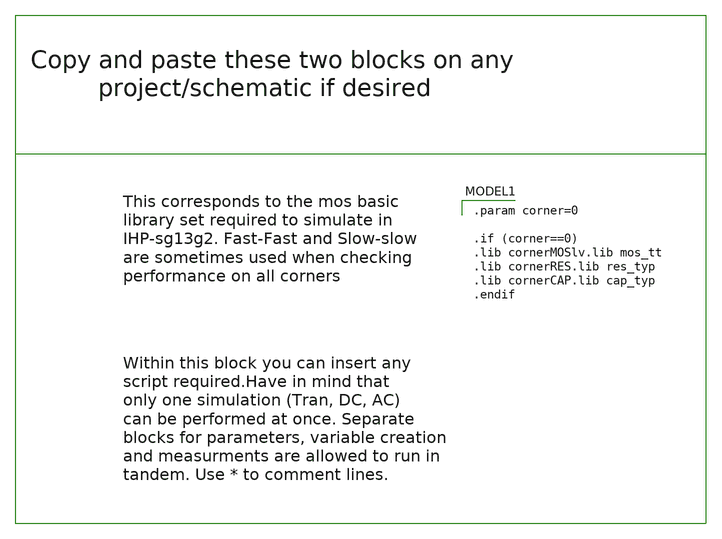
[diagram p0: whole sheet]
** sch_path: Tutoriales/Simulation_fundamentals.sch
**.subckt Simulation_fundamentals
**** begin user architecture code
 .param corner=0

.if (corner==0)
.lib cornerMOSlv.lib mos_tt
.lib cornerRES.lib res_typ
.lib cornerCAP.lib cap_typ
.endif




*At this point the script is to be written. Before the .control command, you can
* Declare Netlist components
* Declare parameters for later use
* Set voltage sources
* Passive loads, can be capacitances or resistors.

.control

*From this point forward, until endc all code will correspond to the simulation script.
*Here, variables can be created through ,let
*Measurments can be aquired, plots be created
*Setting the type of simulation and how it runs.
*The MOST importat part is the latter, since most things that dont include setting
*the simulation can be called for within the simulation console.


save all

*It is convenient to save all parameters at once instead of cherry-picking those you might need.

.endc


.end


**** end user architecture code
**.ends
.end
